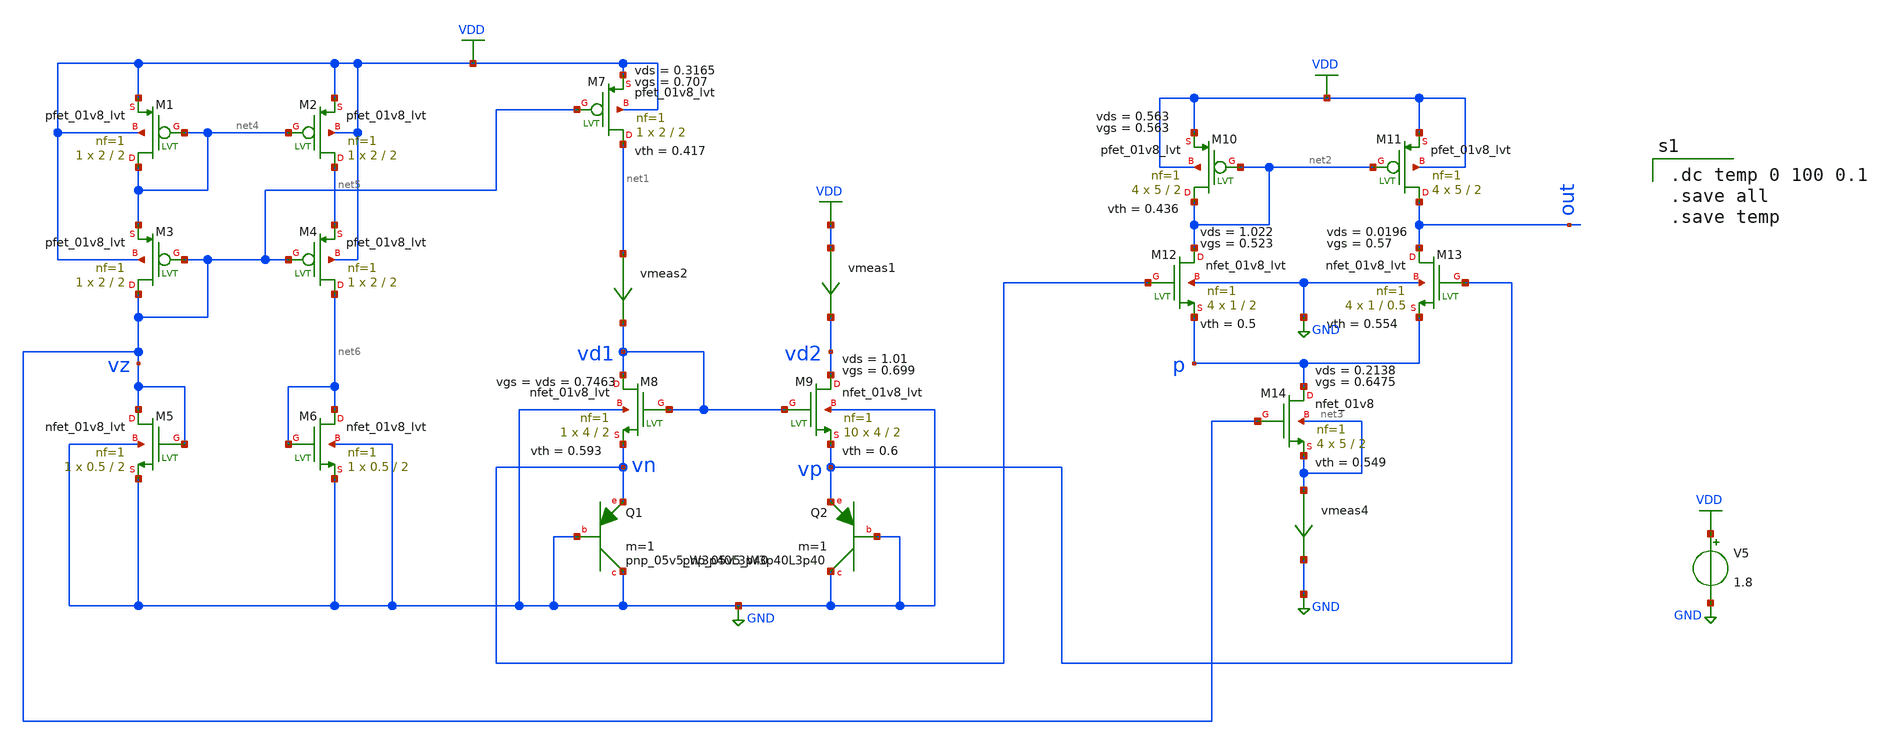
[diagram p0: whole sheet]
** sch_path: XSCHEM/Temp_Sensor_unbalanced_tb.sch
**.subckt Temp_Sensor_unbalanced_tb
V5 VDD GND 1.8
XM8 vd1 vd1 vn GND sky130_fd_pr__nfet_01v8_lvt L=2 W=4 nf=1 ad='int((nf+1)/2) * W/nf * 0.29' as='int((nf+2)/2) * W/nf * 0.29'
+ pd='2*int((nf+1)/2) * (W/nf + 0.29)' ps='2*int((nf+2)/2) * (W/nf + 0.29)' nrd='0.29 / W' nrs='0.29 / W'
+ sa=0 sb=0 sd=0 mult=1 m=1
XQ1 GND GND vn sky130_fd_pr__pnp_05v5_W3p40L3p40 m=1
XM9 vd2 vd1 vp GND sky130_fd_pr__nfet_01v8_lvt L=2 W=4 nf=1 ad='int((nf+1)/2) * W/nf * 0.29' as='int((nf+2)/2) * W/nf * 0.29'
+ pd='2*int((nf+1)/2) * (W/nf + 0.29)' ps='2*int((nf+2)/2) * (W/nf + 0.29)' nrd='0.29 / W' nrs='0.29 / W'
+ sa=0 sb=0 sd=0 mult=10 m=10
XQ2 GND GND vp sky130_fd_pr__pnp_05v5_W3p40L3p40 m=1
vmeas1 VDD vd2 0
.save i(vmeas1)
vmeas2 net1 vd1 0
.save i(vmeas2)
XM7 net1 vz VDD VDD sky130_fd_pr__pfet_01v8_lvt L=2 W=2 nf=1 ad='int((nf+1)/2) * W/nf * 0.29' as='int((nf+2)/2) * W/nf * 0.29'
+ pd='2*int((nf+1)/2) * (W/nf + 0.29)' ps='2*int((nf+2)/2) * (W/nf + 0.29)' nrd='0.29 / W' nrs='0.29 / W'
+ sa=0 sb=0 sd=0 mult=1 m=1
XM12 net2 vn p GND sky130_fd_pr__nfet_01v8_lvt L=2 W=1 nf=1 ad='int((nf+1)/2) * W/nf * 0.29' as='int((nf+2)/2) * W/nf * 0.29'
+ pd='2*int((nf+1)/2) * (W/nf + 0.29)' ps='2*int((nf+2)/2) * (W/nf + 0.29)' nrd='0.29 / W' nrs='0.29 / W'
+ sa=0 sb=0 sd=0 mult=4 m=4
XM13 out vp p GND sky130_fd_pr__nfet_01v8_lvt L=0.5 W=1 nf=1 ad='int((nf+1)/2) * W/nf * 0.29' as='int((nf+2)/2) * W/nf * 0.29'
+ pd='2*int((nf+1)/2) * (W/nf + 0.29)' ps='2*int((nf+2)/2) * (W/nf + 0.29)' nrd='0.29 / W' nrs='0.29 / W'
+ sa=0 sb=0 sd=0 mult=4 m=4
vmeas4 net3 GND 0
.save i(vmeas4)
XM14 p vz net3 net3 sky130_fd_pr__nfet_01v8 L=2 W=5 nf=1 ad='int((nf+1)/2) * W/nf * 0.29' as='int((nf+2)/2) * W/nf * 0.29'
+ pd='2*int((nf+1)/2) * (W/nf + 0.29)' ps='2*int((nf+2)/2) * (W/nf + 0.29)' nrd='0.29 / W' nrs='0.29 / W'
+ sa=0 sb=0 sd=0 mult=4 m=4
XM10 net2 net2 VDD VDD sky130_fd_pr__pfet_01v8_lvt L=2 W=5 nf=1 ad='int((nf+1)/2) * W/nf * 0.29' as='int((nf+2)/2) * W/nf * 0.29'
+ pd='2*int((nf+1)/2) * (W/nf + 0.29)' ps='2*int((nf+2)/2) * (W/nf + 0.29)' nrd='0.29 / W' nrs='0.29 / W'
+ sa=0 sb=0 sd=0 mult=4 m=4
XM11 out net2 VDD VDD sky130_fd_pr__pfet_01v8_lvt L=2 W=5 nf=1 ad='int((nf+1)/2) * W/nf * 0.29' as='int((nf+2)/2) * W/nf * 0.29'
+ pd='2*int((nf+1)/2) * (W/nf + 0.29)' ps='2*int((nf+2)/2) * (W/nf + 0.29)' nrd='0.29 / W' nrs='0.29 / W'
+ sa=0 sb=0 sd=0 mult=4 m=4
XM1 net4 net4 VDD VDD sky130_fd_pr__pfet_01v8_lvt L=2 W=2 nf=1 ad='int((nf+1)/2) * W/nf * 0.29' as='int((nf+2)/2) * W/nf * 0.29'
+ pd='2*int((nf+1)/2) * (W/nf + 0.29)' ps='2*int((nf+2)/2) * (W/nf + 0.29)' nrd='0.29 / W' nrs='0.29 / W'
+ sa=0 sb=0 sd=0 mult=1 m=1
XM5 vz vz GND GND sky130_fd_pr__nfet_01v8_lvt L=2 W=0.5 nf=1 ad='int((nf+1)/2) * W/nf * 0.29' as='int((nf+2)/2) * W/nf * 0.29'
+ pd='2*int((nf+1)/2) * (W/nf + 0.29)' ps='2*int((nf+2)/2) * (W/nf + 0.29)' nrd='0.29 / W' nrs='0.29 / W'
+ sa=0 sb=0 sd=0 mult=1 m=1
XM2 net5 net4 VDD VDD sky130_fd_pr__pfet_01v8_lvt L=2 W=2 nf=1 ad='int((nf+1)/2) * W/nf * 0.29' as='int((nf+2)/2) * W/nf * 0.29'
+ pd='2*int((nf+1)/2) * (W/nf + 0.29)' ps='2*int((nf+2)/2) * (W/nf + 0.29)' nrd='0.29 / W' nrs='0.29 / W'
+ sa=0 sb=0 sd=0 mult=1 m=1
XM4 net6 vz net5 VDD sky130_fd_pr__pfet_01v8_lvt L=2 W=2 nf=1 ad='int((nf+1)/2) * W/nf * 0.29' as='int((nf+2)/2) * W/nf * 0.29'
+ pd='2*int((nf+1)/2) * (W/nf + 0.29)' ps='2*int((nf+2)/2) * (W/nf + 0.29)' nrd='0.29 / W' nrs='0.29 / W'
+ sa=0 sb=0 sd=0 mult=1 m=1
XM3 vz vz net4 VDD sky130_fd_pr__pfet_01v8_lvt L=2 W=2 nf=1 ad='int((nf+1)/2) * W/nf * 0.29' as='int((nf+2)/2) * W/nf * 0.29'
+ pd='2*int((nf+1)/2) * (W/nf + 0.29)' ps='2*int((nf+2)/2) * (W/nf + 0.29)' nrd='0.29 / W' nrs='0.29 / W'
+ sa=0 sb=0 sd=0 mult=1 m=1
XM6 net6 net6 GND GND sky130_fd_pr__nfet_01v8_lvt L=2 W=0.5 nf=1 ad='int((nf+1)/2) * W/nf * 0.29' as='int((nf+2)/2) * W/nf * 0.29'
+ pd='2*int((nf+1)/2) * (W/nf + 0.29)' ps='2*int((nf+2)/2) * (W/nf + 0.29)' nrd='0.29 / W' nrs='0.29 / W'
+ sa=0 sb=0 sd=0 mult=1 m=1
**** begin user architecture code

** opencircuitdesign pdks install
.lib $::SKYWATER_MODELS/sky130.lib.spice tt



.dc temp 0 100 0.1
.save all
.save temp

**** end user architecture code
**.ends
.GLOBAL VDD
.GLOBAL GND
.end
